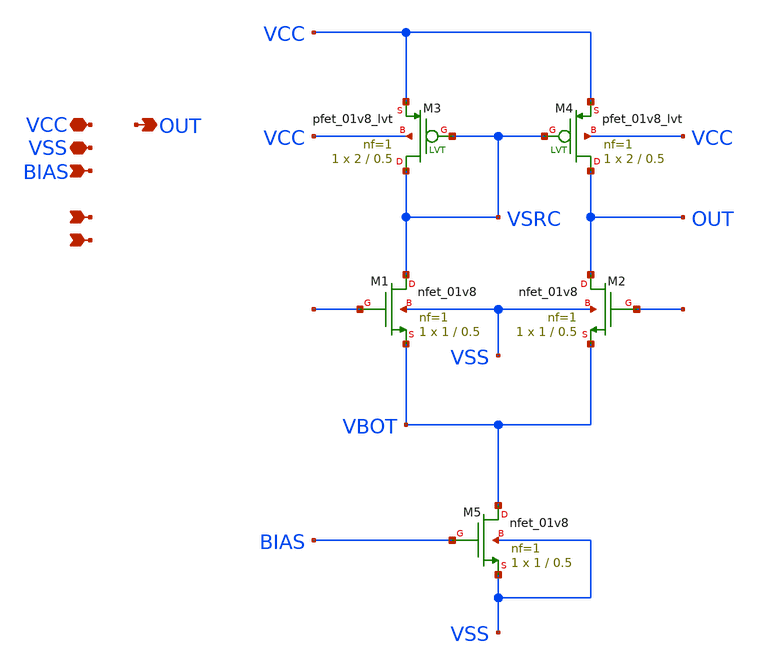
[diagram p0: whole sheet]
** sch_path: schem/ota/ota.sch
**.subckt ota BIAS + - OUT VCC VSS
*.ipin BIAS
*.ipin +
*.ipin -
*.opin OUT
*.iopin VCC
*.iopin VSS
XM1 VSRC + VBOT VSS sky130_fd_pr__nfet_01v8 L=0.5 W=1 nf=1 ad='int((1 + 1)/2) * 1 / 1 * 0.29' as='int((1 + 2)/2) * 1 / 1 * 0.29'
+ pd='2*int((1 + 1)/2) * (1 / 1 + 0.29)' ps='2*int((1 + 2)/2) * (1 / 1 + 0.29)' nrd='0.29 / 1 ' nrs='0.29 / 1 '
+ sa=0 sb=0 sd=0 mult=1 m=1
XM2 OUT - VBOT VSS sky130_fd_pr__nfet_01v8 L=0.5 W=1 nf=1 ad='int((1 + 1)/2) * 1 / 1 * 0.29' as='int((1 + 2)/2) * 1 / 1 * 0.29'
+ pd='2*int((1 + 1)/2) * (1 / 1 + 0.29)' ps='2*int((1 + 2)/2) * (1 / 1 + 0.29)' nrd='0.29 / 1 ' nrs='0.29 / 1 '
+ sa=0 sb=0 sd=0 mult=1 m=1
XM3 VSRC VSRC VCC VCC sky130_fd_pr__pfet_01v8_lvt L=0.5 W=2 nf=1 ad='int((1 + 1)/2) * 2 / 1 * 0.29' as='int((1 + 2)/2) * 2 / 1 * 0.29'
+ pd='2*int((1 + 1)/2) * (2 / 1 + 0.29)' ps='2*int((1 + 2)/2) * (2 / 1 + 0.29)' nrd='0.29 / 2 ' nrs='0.29 / 2 '
+ sa=0 sb=0 sd=0 mult=1 m=1
XM4 OUT VSRC VCC VCC sky130_fd_pr__pfet_01v8_lvt L=0.5 W=2 nf=1 ad='int((1 + 1)/2) * 2 / 1 * 0.29' as='int((1 + 2)/2) * 2 / 1 * 0.29'
+ pd='2*int((1 + 1)/2) * (2 / 1 + 0.29)' ps='2*int((1 + 2)/2) * (2 / 1 + 0.29)' nrd='0.29 / 2 ' nrs='0.29 / 2 '
+ sa=0 sb=0 sd=0 mult=1 m=1
XM5 VBOT BIAS VSS VSS sky130_fd_pr__nfet_01v8 L=0.5 W=1 nf=1 ad='int((1 + 1)/2) * 1 / 1 * 0.29' as='int((1 + 2)/2) * 1 / 1 * 0.29'
+ pd='2*int((1 + 1)/2) * (1 / 1 + 0.29)' ps='2*int((1 + 2)/2) * (1 / 1 + 0.29)' nrd='0.29 / 1 ' nrs='0.29 / 1 '
+ sa=0 sb=0 sd=0 mult=1 m=1
**.ends
.end
